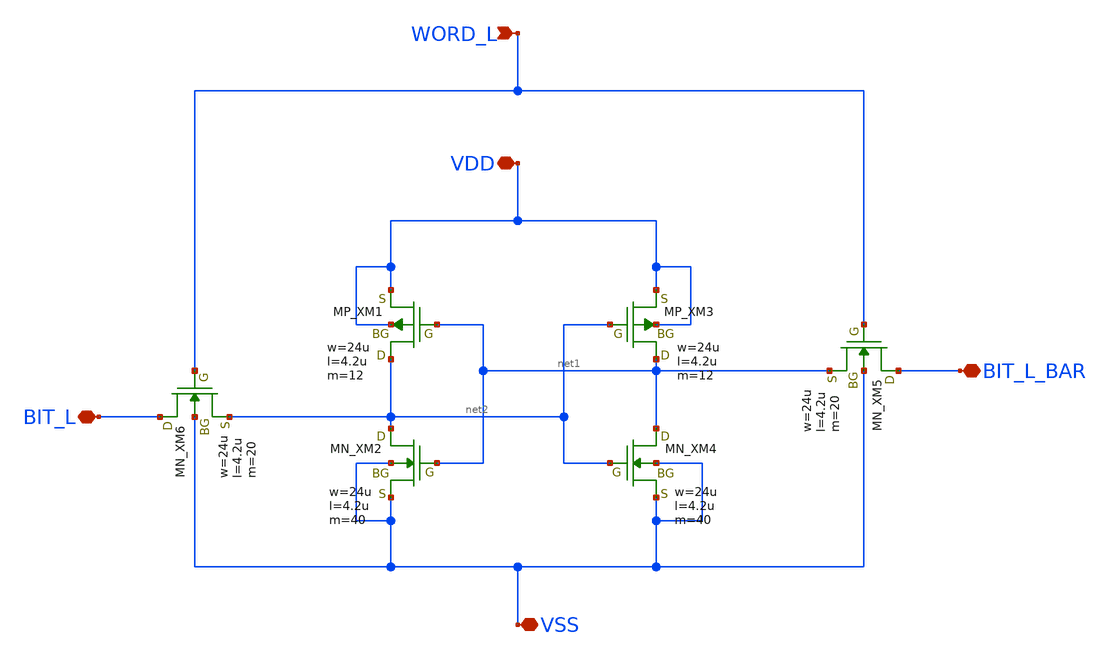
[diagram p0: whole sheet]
** sch_path: member_project/SRAM/noritsuna/1bit_sram.sch
**.subckt 1bit_sram VDD VSS BIT_L_BAR BIT_L WORD_L
*.iopin VDD
*.iopin VSS
*.iopin BIT_L_BAR
*.iopin BIT_L
*.ipin WORD_L
XXM1 net2 net1 VDD VDD PMOS w=24u l=4.2u nrd=0 nrs=0 m=12
XXM2 net2 net1 VSS VSS NMOS w=24u l=4.2u nrd=0 nrs=0 m=40
XXM3 net1 net2 VDD VDD PMOS w=24u l=4.2u nrd=0 nrs=0 m=12
XXM4 net1 net2 VSS VSS NMOS w=24u l=4.2u nrd=0 nrs=0 m=40
XXM5 BIT_L_BAR WORD_L net1 VSS NMOS w=24u l=4.2u nrd=0 nrs=0 m=20
XXM6 BIT_L WORD_L net2 VSS NMOS w=24u l=4.2u nrd=0 nrs=0 m=20
**.ends
.end
